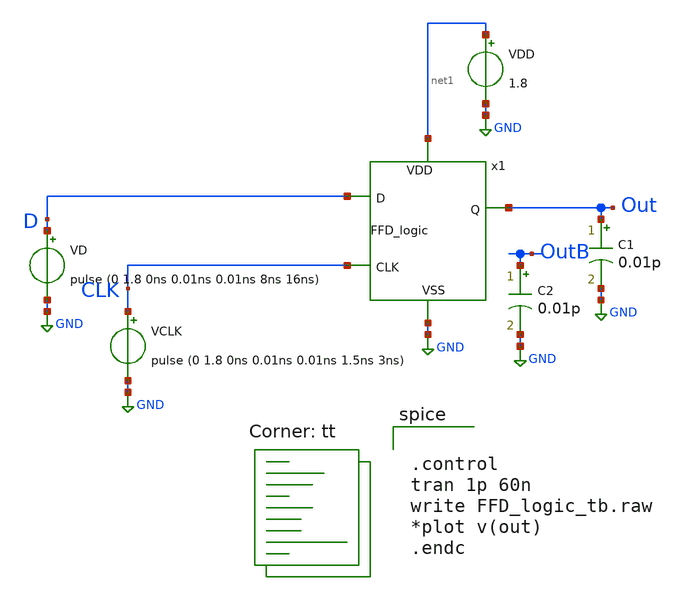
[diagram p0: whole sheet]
** sch_path: FFD_logic_tb.sch
**.subckt FFD_logic_tb
VD D GND pulse (0 1.8 0ns 0.01ns 0.01ns 8ns 16ns)
VCLK CLK GND pulse (0 1.8 0ns 0.01ns 0.01ns 1.5ns 3ns)
VDD net1 GND 1.8
C1 Out GND 0.01p m=1
C2 OutB GND 0.01p m=1
x1 Out D net1 CLK GND FFD_logic
**** begin user architecture code
.lib $::SKYWATER_MODELS/sky130.lib.spice tt


.control
tran 1p 60n
write FFD_logic_tb.raw
*plot v(out)
.endc


**** end user architecture code
**.ends

* expanding   symbol:  project/FFD_logic.sym # of pins=5
** sym_path: FFD_logic.sym
** sch_path: FFD_logic.sch
.subckt FFD_logic Q D VDD CLK VSS
*.ipin D
*.ipin CLK
*.ipin VDD
*.ipin VSS
*.opin Q
x1 VDD net3 D net2 VSS nand_FFD
x2 VDD net4 net2 net1 VSS nand_FFD
x3 VDD net5 net3 net6 VSS nand_FFD
x4 VDD net6 net5 net4 VSS nand_FFD
x5 VDD net8 net5 CLK VSS nand_FFD
x6 VDD net7 CLK net6 VSS nand_FFD
x7 VDD Q net8 net9 VSS nand_FFD
x8 VDD net9 Q net7 VSS nand_FFD
x9 VDD D net1 VSS Inverter
x10 VDD CLK net2 VSS Inverter
.ends


* expanding   symbol:  nand_FFD.sym # of pins=5
** sym_path: nand_FFD.sym
** sch_path: nand_FFD.sch
.subckt nand_FFD VDD Y A B VSS
*.ipin VDD
*.ipin A
*.ipin B
*.ipin VSS
*.opin Y
XM1 Y A net1 VSS sky130_fd_pr__nfet_01v8 L=0.15 W=1 nf=1 ad='int((nf+1)/2) * W/nf * 0.29' as='int((nf+2)/2) * W/nf * 0.29'
+ pd='2*int((nf+1)/2) * (W/nf + 0.29)' ps='2*int((nf+2)/2) * (W/nf + 0.29)' nrd='0.29 / W' nrs='0.29 / W'
+ sa=0 sb=0 sd=0 mult=1 m=1
XM2 net1 B VSS VSS sky130_fd_pr__nfet_01v8 L=0.15 W=1 nf=1 ad='int((nf+1)/2) * W/nf * 0.29' as='int((nf+2)/2) * W/nf * 0.29'
+ pd='2*int((nf+1)/2) * (W/nf + 0.29)' ps='2*int((nf+2)/2) * (W/nf + 0.29)' nrd='0.29 / W' nrs='0.29 / W'
+ sa=0 sb=0 sd=0 mult=1 m=1
XM3 Y A VDD VDD sky130_fd_pr__pfet_01v8 L=0.15 W=2 nf=1 ad='int((nf+1)/2) * W/nf * 0.29' as='int((nf+2)/2) * W/nf * 0.29'
+ pd='2*int((nf+1)/2) * (W/nf + 0.29)' ps='2*int((nf+2)/2) * (W/nf + 0.29)' nrd='0.29 / W' nrs='0.29 / W'
+ sa=0 sb=0 sd=0 mult=1 m=1
XM4 Y B VDD VDD sky130_fd_pr__pfet_01v8 L=0.15 W=2 nf=1 ad='int((nf+1)/2) * W/nf * 0.29' as='int((nf+2)/2) * W/nf * 0.29'
+ pd='2*int((nf+1)/2) * (W/nf + 0.29)' ps='2*int((nf+2)/2) * (W/nf + 0.29)' nrd='0.29 / W' nrs='0.29 / W'
+ sa=0 sb=0 sd=0 mult=1 m=1
.ends


* expanding   symbol:  Inverter.sym # of pins=4
** sym_path: Inverter.sym
** sch_path: Inverter.sch
.subckt Inverter VDD IN OUT VSS
*.ipin IN
*.ipin VSS
*.ipin VDD
*.opin OUT
XM1 OUT IN VSS VSS sky130_fd_pr__nfet_01v8 L=0.3 W=1 nf=1 ad='int((nf+1)/2) * W/nf * 0.29' as='int((nf+2)/2) * W/nf * 0.29'
+ pd='2*int((nf+1)/2) * (W/nf + 0.29)' ps='2*int((nf+2)/2) * (W/nf + 0.29)' nrd='0.29 / W' nrs='0.29 / W'
+ sa=0 sb=0 sd=0 mult=1 m=1
XM2 OUT IN VDD VDD sky130_fd_pr__pfet_01v8 L=0.3 W=2 nf=1 ad='int((nf+1)/2) * W/nf * 0.29' as='int((nf+2)/2) * W/nf * 0.29'
+ pd='2*int((nf+1)/2) * (W/nf + 0.29)' ps='2*int((nf+2)/2) * (W/nf + 0.29)' nrd='0.29 / W' nrs='0.29 / W'
+ sa=0 sb=0 sd=0 mult=1 m=1
.ends

.GLOBAL GND
.end
